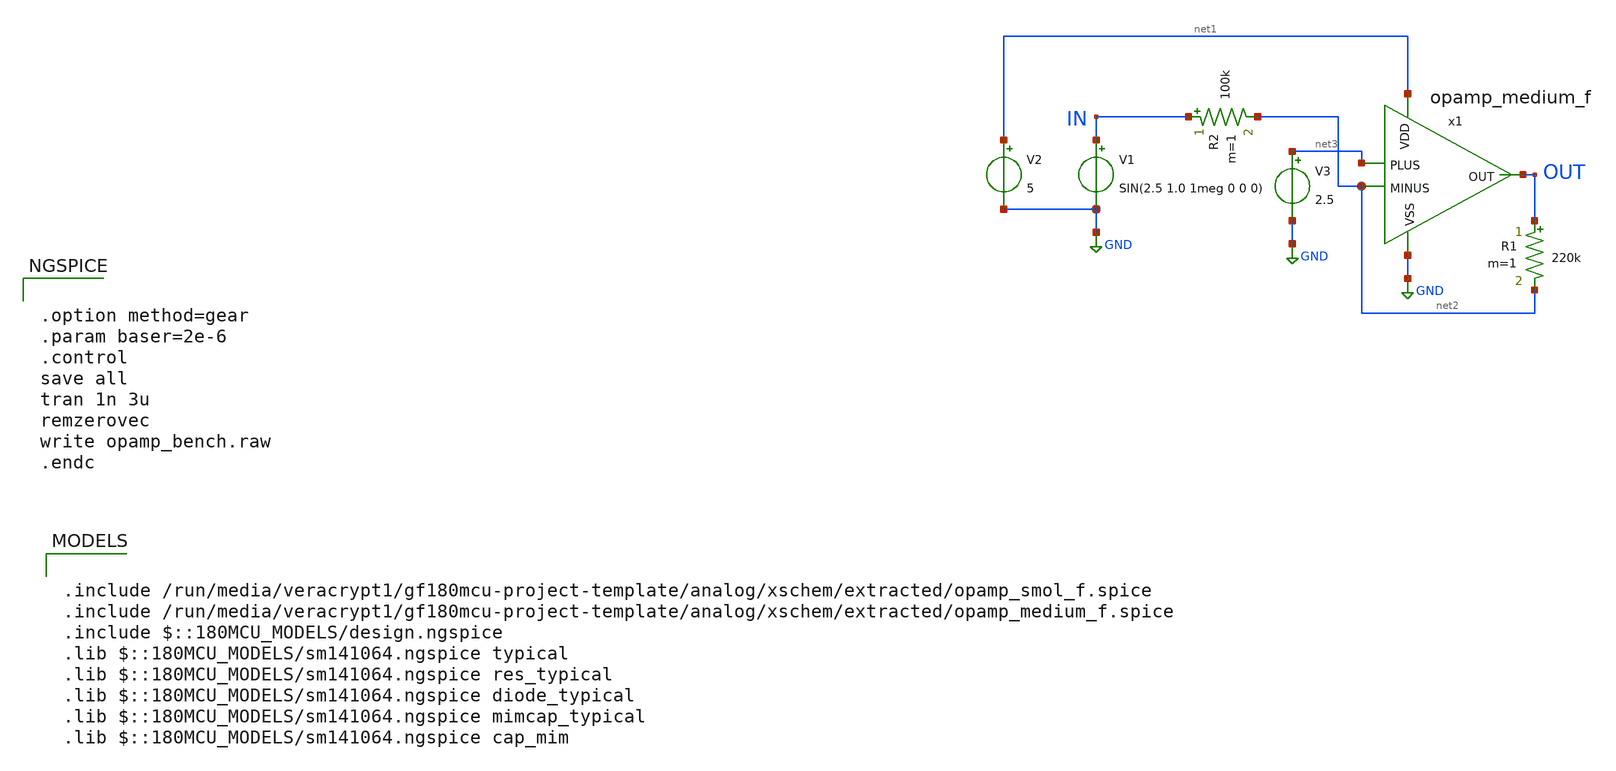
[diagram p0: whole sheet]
** sch_path: analog/xschem/opamp_bench.sch
**.subckt opamp_bench
V1 IN GND SIN(2.5 1.0 1meg 0 0 0)
V2 net1 GND 5
R1 OUT net2 220k m=1
V3 net3 GND 2.5
R2 IN net2 100k m=1
x1 net1 GND net2 net3 OUT opamp_medium_f
**** begin user architecture code


.option method=gear
.param baser=2e-6
.control
save all
tran 1n 3u
remzerovec
write opamp_bench.raw
.endc



.include /run/media/veracrypt1/gf180mcu-project-template/analog/xschem/extracted/opamp_smol_f.spice
.include /run/media/veracrypt1/gf180mcu-project-template/analog/xschem/extracted/opamp_medium_f.spice
.include $::180MCU_MODELS/design.ngspice
.lib $::180MCU_MODELS/sm141064.ngspice typical
.lib $::180MCU_MODELS/sm141064.ngspice res_typical
.lib $::180MCU_MODELS/sm141064.ngspice diode_typical
.lib $::180MCU_MODELS/sm141064.ngspice mimcap_typical
.lib $::180MCU_MODELS/sm141064.ngspice cap_mim

**** end user architecture code
**.ends
.GLOBAL GND
.end
